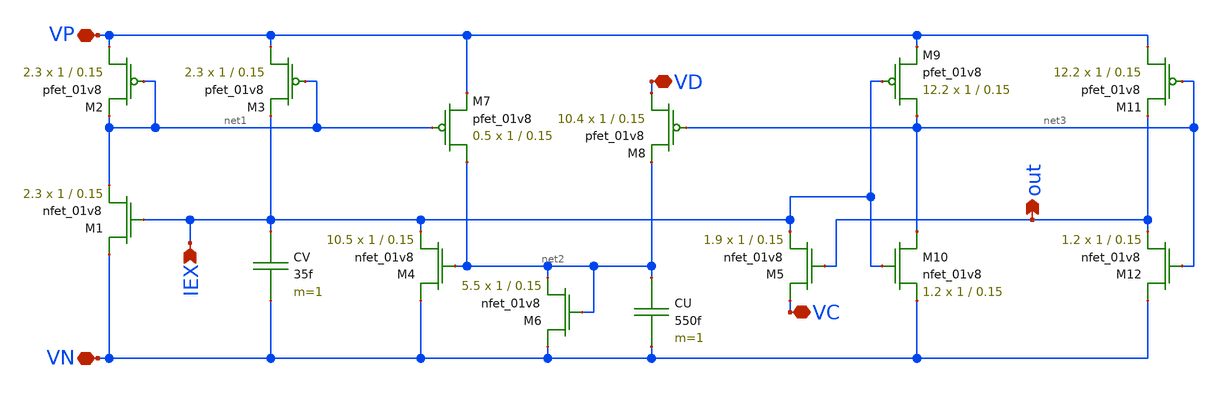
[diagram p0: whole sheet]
** sch_path: schematic/ronchini_neuron.sch
**.subckt ronchini_neuron VN VP IEX VD VC out
*.iopin VN
*.iopin VP
*.ipin IEX
*.iopin VD
*.iopin VC
*.opin out
CV IEX VN 35f m=1
CU net2 VN 550f m=1
XM7 net2 net1 VP VDD sky130_fd_pr__pfet_01v8 L=0.15 W=1 nf=1 ad='int((nf+1)/2) * W/nf * 0.29' as='int((nf+2)/2) * W/nf * 0.29'
+ pd='2*int((nf+1)/2) * (W/nf + 0.29)' ps='2*int((nf+2)/2) * (W/nf + 0.29)' nrd='0.29 / W' nrs='0.29 / W'
+ sa=0 sb=0 sd=0 mult=0.5 m=0.5
XM8 VD net3 net2 VDD sky130_fd_pr__pfet_01v8 L=0.15 W=1 nf=1 ad='int((nf+1)/2) * W/nf * 0.29' as='int((nf+2)/2) * W/nf * 0.29'
+ pd='2*int((nf+1)/2) * (W/nf + 0.29)' ps='2*int((nf+2)/2) * (W/nf + 0.29)' nrd='0.29 / W' nrs='0.29 / W'
+ sa=0 sb=0 sd=0 mult=10.4 m=10.4
XM10 net3 IEX VN GND sky130_fd_pr__nfet_01v8 L=0.15 W=1 nf=1 ad='int((nf+1)/2) * W/nf * 0.29' as='int((nf+2)/2) * W/nf * 0.29'
+ pd='2*int((nf+1)/2) * (W/nf + 0.29)' ps='2*int((nf+2)/2) * (W/nf + 0.29)' nrd='0.29 / W' nrs='0.29 / W'
+ sa=0 sb=0 sd=0 mult=1.2 m=1.2
XM12 VN net3 out GND sky130_fd_pr__nfet_01v8 L=0.15 W=1 nf=1 ad='int((nf+1)/2) * W/nf * 0.29' as='int((nf+2)/2) * W/nf * 0.29'
+ pd='2*int((nf+1)/2) * (W/nf + 0.29)' ps='2*int((nf+2)/2) * (W/nf + 0.29)' nrd='0.29 / W' nrs='0.29 / W'
+ sa=0 sb=0 sd=0 mult=1.2 m=1.2
XM5 VC out IEX GND sky130_fd_pr__nfet_01v8 L=0.15 W=1 nf=1 ad='int((nf+1)/2) * W/nf * 0.29' as='int((nf+2)/2) * W/nf * 0.29'
+ pd='2*int((nf+1)/2) * (W/nf + 0.29)' ps='2*int((nf+2)/2) * (W/nf + 0.29)' nrd='0.29 / W' nrs='0.29 / W'
+ sa=0 sb=0 sd=0 mult=1.9 m=1.9
XM2 VP net1 net1 VDD sky130_fd_pr__pfet_01v8 L=0.15 W=1 nf=1 ad='int((nf+1)/2) * W/nf * 0.29' as='int((nf+2)/2) * W/nf * 0.29'
+ pd='2*int((nf+1)/2) * (W/nf + 0.29)' ps='2*int((nf+2)/2) * (W/nf + 0.29)' nrd='0.29 / W' nrs='0.29 / W'
+ sa=0 sb=0 sd=0 mult=2.3 m=2.3
XM3 VP net1 IEX VDD sky130_fd_pr__pfet_01v8 L=0.15 W=1 nf=1 ad='int((nf+1)/2) * W/nf * 0.29' as='int((nf+2)/2) * W/nf * 0.29'
+ pd='2*int((nf+1)/2) * (W/nf + 0.29)' ps='2*int((nf+2)/2) * (W/nf + 0.29)' nrd='0.29 / W' nrs='0.29 / W'
+ sa=0 sb=0 sd=0 mult=2.3 m=2.3
XM1 VN IEX net1 GND sky130_fd_pr__nfet_01v8 L=0.15 W=1 nf=1 ad='int((nf+1)/2) * W/nf * 0.29' as='int((nf+2)/2) * W/nf * 0.29'
+ pd='2*int((nf+1)/2) * (W/nf + 0.29)' ps='2*int((nf+2)/2) * (W/nf + 0.29)' nrd='0.29 / W' nrs='0.29 / W'
+ sa=0 sb=0 sd=0 mult=2.3 m=2.3
XM4 VN net2 IEX GND sky130_fd_pr__nfet_01v8 L=0.15 W=1 nf=1 ad='int((nf+1)/2) * W/nf * 0.29' as='int((nf+2)/2) * W/nf * 0.29'
+ pd='2*int((nf+1)/2) * (W/nf + 0.29)' ps='2*int((nf+2)/2) * (W/nf + 0.29)' nrd='0.29 / W' nrs='0.29 / W'
+ sa=0 sb=0 sd=0 mult=10.5 m=10.5
XM6 VN net2 net2 GND sky130_fd_pr__nfet_01v8 L=0.15 W=1 nf=1 ad='int((nf+1)/2) * W/nf * 0.29' as='int((nf+2)/2) * W/nf * 0.29'
+ pd='2*int((nf+1)/2) * (W/nf + 0.29)' ps='2*int((nf+2)/2) * (W/nf + 0.29)' nrd='0.29 / W' nrs='0.29 / W'
+ sa=0 sb=0 sd=0 mult=5.5 m=5.5
XM9 net3 IEX VP VDD sky130_fd_pr__pfet_01v8 L=0.15 W=1 nf=1 ad='int((nf+1)/2) * W/nf * 0.29' as='int((nf+2)/2) * W/nf * 0.29'
+ pd='2*int((nf+1)/2) * (W/nf + 0.29)' ps='2*int((nf+2)/2) * (W/nf + 0.29)' nrd='0.29 / W' nrs='0.29 / W'
+ sa=0 sb=0 sd=0 mult=12.2 m=12.2
XM11 VP net3 out VDD sky130_fd_pr__pfet_01v8 L=0.15 W=1 nf=1 ad='int((nf+1)/2) * W/nf * 0.29' as='int((nf+2)/2) * W/nf * 0.29'
+ pd='2*int((nf+1)/2) * (W/nf + 0.29)' ps='2*int((nf+2)/2) * (W/nf + 0.29)' nrd='0.29 / W' nrs='0.29 / W'
+ sa=0 sb=0 sd=0 mult=12.2 m=12.2
**.ends
.end
